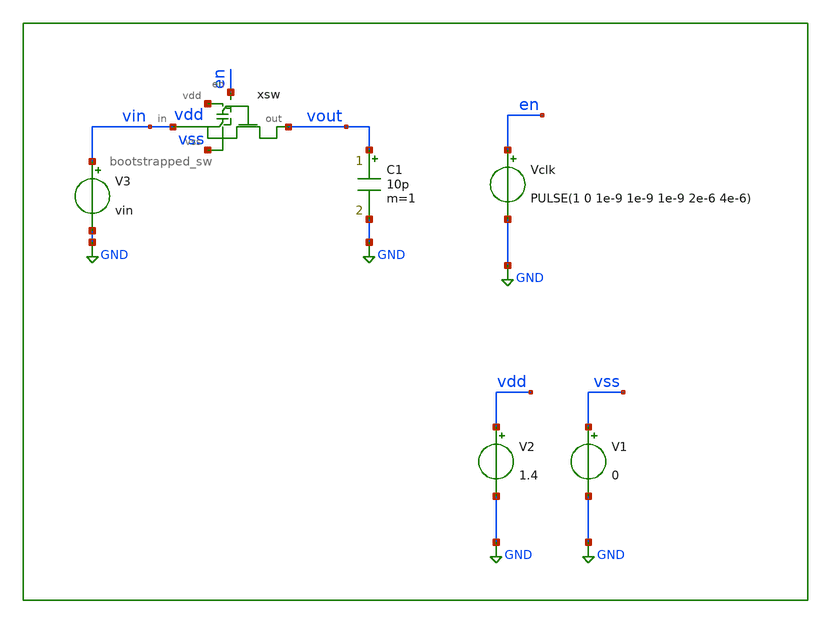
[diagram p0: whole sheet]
** sch_path: xschem/tb/switches/tr_bootstrapped_sw.sch
**.subckt tr_bootstrapped_sw
V1 vss GND 0
V2 vdd GND 1.4
Vclk en GND PULSE(1 0 1e-9 1e-9 1e-9 2e-6 4e-6)
C1 vout GND 10p m=1
V3 vin GND vin
xsw vout en vdd vin vss bootstrapped_sw
**** begin user architecture code
 *.options method trap
*.options gmin 1e-15
*.options abstol 1e-15
*.options reltol 0.0001
*.options vntol 0.1e-6
*
.include $::DESIGN_PATH/switches/bootstrapped_sw.sp

.param vin=0.7
.param MC_SWITCH=0

*.tran 100e-9 4e-6
.temp 85

.control
save all
tran 100e-9 16e-6 uic
run


* settle values
meas tran vset find v(vout) at=3.99e-6
meas tran vg_end find v(xsw.vg) at=3.99e-6
meas tran vin_end find v(vin) at=3.99e-6

let vgs_end=vg_end-vin_end

* max values
meas tran vg_max max xsw.vg
meas tran vs_max max xsw.vs
meas tran vbsl_max max xsw.vbsl
meas tran vbsh_max max xsw.vbsh

* min values
meas tran vg_min min xsw.vg
meas tran vs_min min xsw.vs
meas tran vbsl_min min xsw.vbsl
meas tran vbsh_min min xsw.vbsh


* print results
print vset
print vgs_end

print vg_max
print vs_max
print vbsl_max
print vbsh_max
print vg_min
print vs_min
print vbsl_min
print vbsh_min

.endc

 * FET CORNERS
*.include $::SKYWATER_MODELS/corners/tt.spice
.include $::SKYWATER_MODELS/corners/ff.spice
*.include $::SKYWATER_MODELS/corners/ss.spice
*.include $::SKYWATER_MODELS/corners/sf.spice
*.include $::SKYWATER_MODELS/corners/fs.spice

* TT + R + C
*.include $::SKYWATER_MODELS/corners/tt_rmax_cmax.spice
*.include $::SKYWATER_MODELS/corners/tt_rmin_cmin.spice
*.include $::SKYWATER_MODELS/corners/tt_rmax_cmin.spice
*.include $::SKYWATER_MODELS/corners/tt_rmin_cmax.spice

* FF + R + C
*.include $::SKYWATER_MODELS/corners/ff_rmax_cmax.spice
*.include $::SKYWATER_MODELS/corners/ff_rmin_cmin.spice
*.include $::SKYWATER_MODELS/corners/ff_rmax_cmin.spice
*.include $::SKYWATER_MODELS/corners/ff_rmin_cmax.spice


* SS + R + C
*.include $::SKYWATER_MODELS/corners/ss_rmax_cmax.spice
*.include $::SKYWATER_MODELS/corners/ss_rmin_cmin.spice
*.include $::SKYWATER_MODELS/corners/ss_rmax_cmin.spice
*.include $::SKYWATER_MODELS/corners/ss_rmin_cmax.spice

* SF + R + C
*.include $::SKYWATER_MODELS/corners/sf_rmax_cmax.spice
*.include $::SKYWATER_MODELS/corners/sf_rmin_cmin.spice
*.include $::SKYWATER_MODELS/corners/sf_rmax_cmin.spice
*.include $::SKYWATER_MODELS/corners/sf_rmin_cmax.spice

* FS + R + C
*.include $::SKYWATER_MODELS/corners/fs_rmax_cmax.spice
*.include $::SKYWATER_MODELS/corners/fs_rmin_cmin.spice
*.include $::SKYWATER_MODELS/corners/fs_rmax_cmin.spice
*.include $::SKYWATER_MODELS/corners/fs_rmin_cmax.spice

**** end user architecture code
**.ends

* expanding   symbol:  switches/bootstrapped_sw.sym # of pins=5
** sym_path: xschem/switches/bootstrapped_sw.sym
** sch_path: xschem/switches/bootstrapped_sw.sch
.subckt bootstrapped_sw out en vdd in vss
*.iopin out
*.ipin en
*.iopin vss
*.iopin vdd
*.iopin in
xinv1 vdd en enb vss inv_lvt
XMs out vg in vss sky130_fd_pr__nfet_01v8_lvt L=0.5 W=1 nf=1 ad='int((nf+1)/2) * W/nf * 0.29' as='int((nf+2)/2) * W/nf * 0.29'
+ pd='2*int((nf+1)/2) * (W/nf + 0.29)' ps='2*int((nf+2)/2) * (W/nf + 0.29)' nrd='0.29 / W' nrs='0.29 / W'
+ sa=0 sb=0 sd=0 mult=1 m=1
XMs1 vs vdd vg vss sky130_fd_pr__nfet_01v8_lvt L=0.4 W=1 nf=1 ad='int((nf+1)/2) * W/nf * 0.29' as='int((nf+2)/2) * W/nf * 0.29'
+ pd='2*int((nf+1)/2) * (W/nf + 0.29)' ps='2*int((nf+2)/2) * (W/nf + 0.29)' nrd='0.29 / W' nrs='0.29 / W'
+ sa=0 sb=0 sd=0 mult=1 m=1
XMs2 vss enb vs vss sky130_fd_pr__nfet_01v8_lvt L=0.4 W=1 nf=1 ad='int((nf+1)/2) * W/nf * 0.29' as='int((nf+2)/2) * W/nf * 0.29'
+ pd='2*int((nf+1)/2) * (W/nf + 0.29)' ps='2*int((nf+2)/2) * (W/nf + 0.29)' nrd='0.29 / W' nrs='0.29 / W'
+ sa=0 sb=0 sd=0 mult=1 m=1
XM4 vg enb vbsh vbsh sky130_fd_pr__pfet_01v8_lvt L=0.4 W=1 nf=1 ad='int((nf+1)/2) * W/nf * 0.29' as='int((nf+2)/2) * W/nf * 0.29'
+ pd='2*int((nf+1)/2) * (W/nf + 0.29)' ps='2*int((nf+2)/2) * (W/nf + 0.29)' nrd='0.29 / W' nrs='0.29 / W'
+ sa=0 sb=0 sd=0 mult=1 m=1
XM1 vbsl vg in vss sky130_fd_pr__nfet_01v8_lvt L=0.4 W=1 nf=1 ad='int((nf+1)/2) * W/nf * 0.29' as='int((nf+2)/2) * W/nf * 0.29'
+ pd='2*int((nf+1)/2) * (W/nf + 0.29)' ps='2*int((nf+2)/2) * (W/nf + 0.29)' nrd='0.29 / W' nrs='0.29 / W'
+ sa=0 sb=0 sd=0 mult=1 m=1
XM2 vbsl enb vss vss sky130_fd_pr__nfet_01v8_lvt L=0.4 W=1 nf=1 ad='int((nf+1)/2) * W/nf * 0.29' as='int((nf+2)/2) * W/nf * 0.29'
+ pd='2*int((nf+1)/2) * (W/nf + 0.29)' ps='2*int((nf+2)/2) * (W/nf + 0.29)' nrd='0.29 / W' nrs='0.29 / W'
+ sa=0 sb=0 sd=0 mult=1 m=1
XM3 vdd vg vbsh vbsh sky130_fd_pr__pfet_01v8_lvt L=0.4 W=1 nf=1 ad='int((nf+1)/2) * W/nf * 0.29' as='int((nf+2)/2) * W/nf * 0.29'
+ pd='2*int((nf+1)/2) * (W/nf + 0.29)' ps='2*int((nf+2)/2) * (W/nf + 0.29)' nrd='0.29 / W' nrs='0.29 / W'
+ sa=0 sb=0 sd=0 mult=1 m=1
XCbs[3] vbsh vbsl sky130_fd_pr__cap_mim_m3_1 W=5 L=5 MF=1 m=1
XCbs[2] vbsh vbsl sky130_fd_pr__cap_mim_m3_1 W=5 L=5 MF=1 m=1
XCbs[1] vbsh vbsl sky130_fd_pr__cap_mim_m3_1 W=5 L=5 MF=1 m=1
XCbs[0] vbsh vbsl sky130_fd_pr__cap_mim_m3_1 W=5 L=5 MF=1 m=1
.ends


* expanding   symbol:  logic/inv_lvt.sym # of pins=4
** sym_path: xschem/logic/inv_lvt.sym
** sch_path: xschem/logic/inv_lvt.sch
.subckt inv_lvt vdd in out vss
*.iopin vdd
*.iopin vss
*.ipin in
*.opin out
XM1 out in vss vss sky130_fd_pr__nfet_01v8_lvt L=0.4 W=1 nf=1 ad='int((nf+1)/2) * W/nf * 0.29' as='int((nf+2)/2) * W/nf * 0.29'
+ pd='2*int((nf+1)/2) * (W/nf + 0.29)' ps='2*int((nf+2)/2) * (W/nf + 0.29)' nrd='0.29 / W' nrs='0.29 / W'
+ sa=0 sb=0 sd=0 mult=1 m=1
XM2 out in vdd vdd sky130_fd_pr__pfet_01v8_lvt L=0.4 W=1 nf=1 ad='int((nf+1)/2) * W/nf * 0.29' as='int((nf+2)/2) * W/nf * 0.29'
+ pd='2*int((nf+1)/2) * (W/nf + 0.29)' ps='2*int((nf+2)/2) * (W/nf + 0.29)' nrd='0.29 / W' nrs='0.29 / W'
+ sa=0 sb=0 sd=0 mult=1 m=1
.ends

.GLOBAL GND
.end
